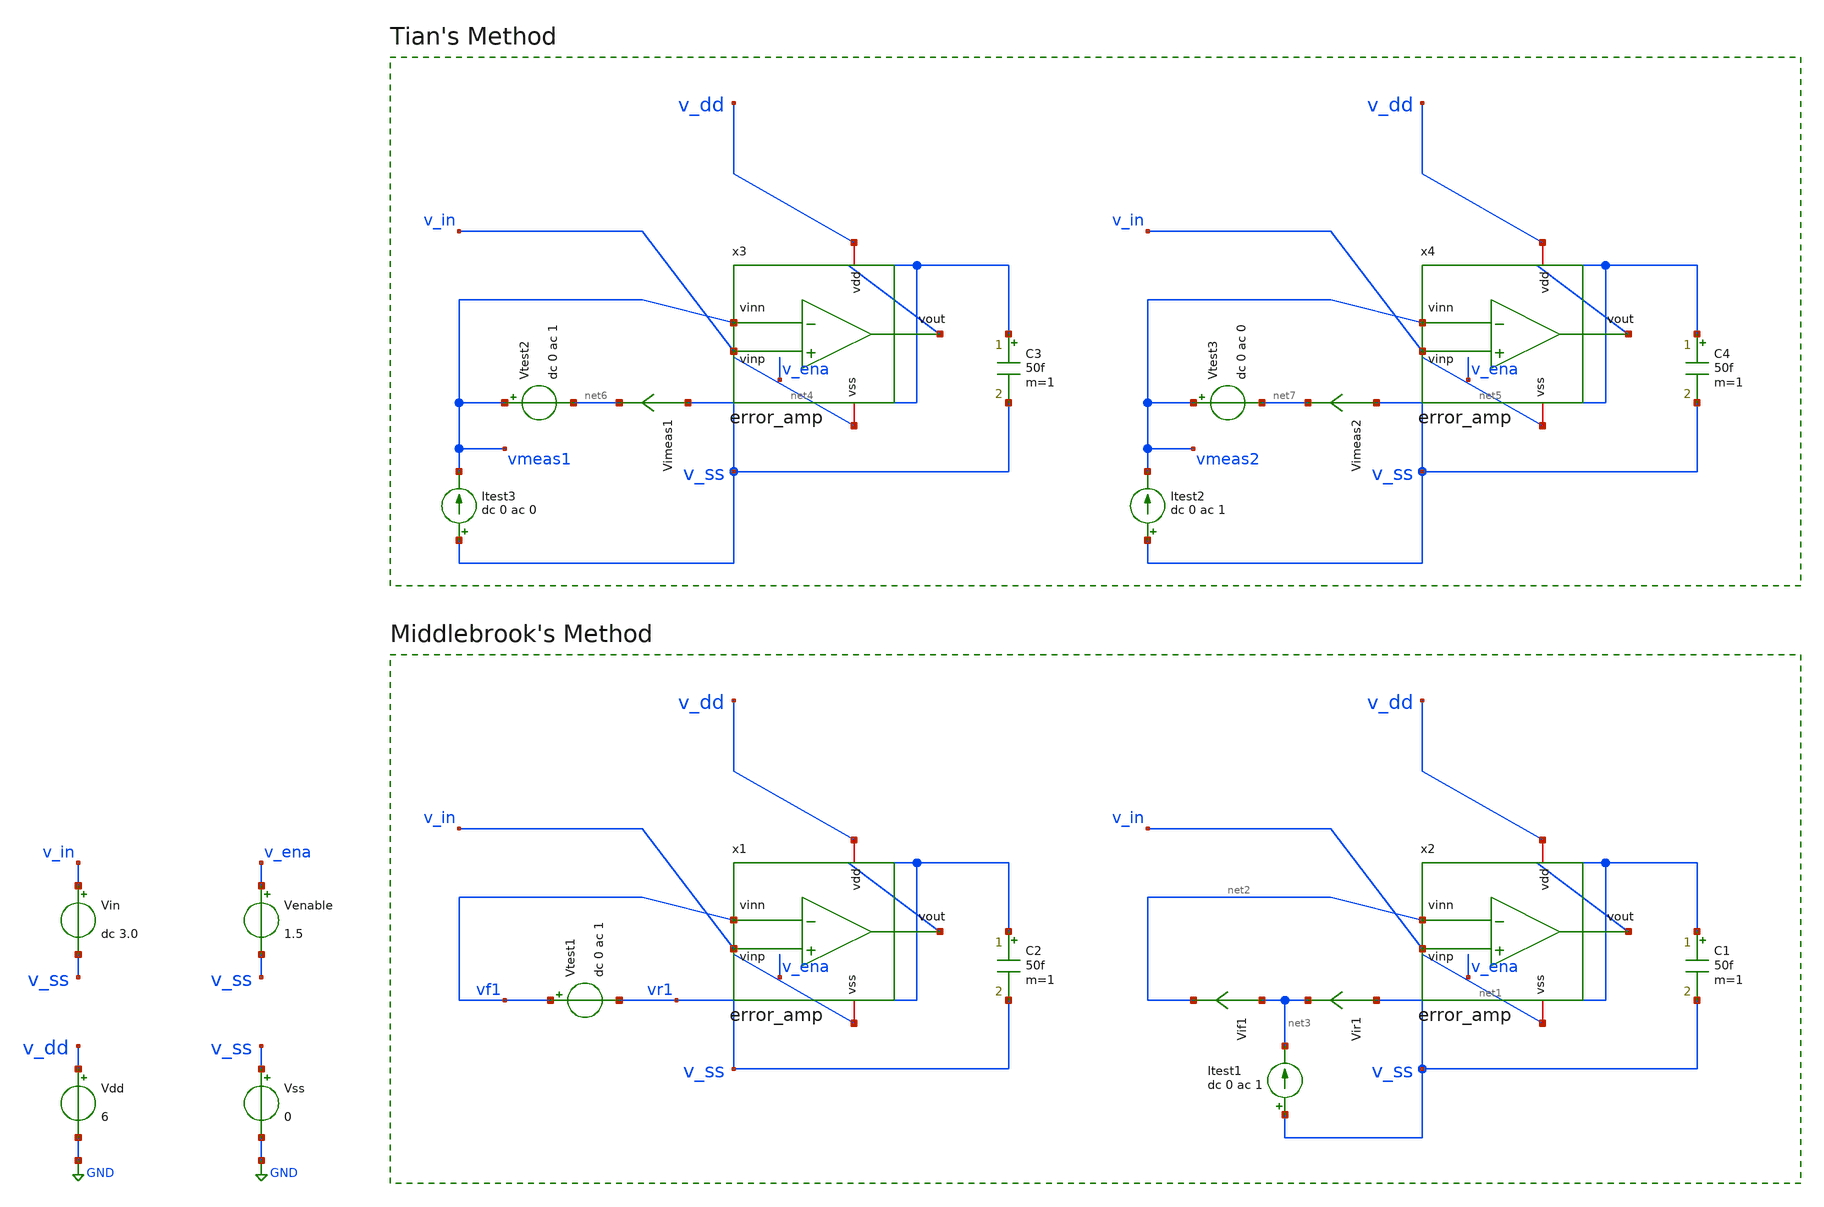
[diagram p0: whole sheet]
** sch_path: analog-db/drawings/ldo-005-ti-ldo-buffer-ref/gf180/error_amp/error_amp_tb-loopgain.sch
* (c) 2024 H. Pretl, S. Dorrer, Apache-2.0 license
**.subckt error_amp_tb-loopgain
Vdd v_dd GND 6
Vss v_ss GND 0
Vin v_in v_ss dc 3.0
Venable v_ena v_ss 1.5
C2 vr1 v_ss 50f m=1
x1 v_dd vr1 v_in vf1 v_ss error_amp
Vtest1 vf1 vr1 dc 0 ac 1
C1 net1 v_ss 50f m=1
x2 v_dd net1 v_in net2 v_ss error_amp
Vir1 net1 net3 0
Vif1 net3 net2 0
Itest1 v_ss net3 dc 0 ac 1
C3 net4 v_ss 50f m=1
x3 v_dd net4 v_in vmeas1 v_ss error_amp
C4 net5 v_ss 50f m=1
x4 v_dd net5 v_in vmeas2 v_ss error_amp
Itest3 v_ss vmeas1 dc 0 ac 0
Vtest2 vmeas1 net6 dc 0 ac 1
Vimeas1 net4 net6 0
Itest2 v_ss vmeas2 dc 0 ac 1
Vtest3 vmeas2 net7 dc 0 ac 0
Vimeas2 net5 net7 0
**** begin user architecture code
 .include $::180MCU_MODELS/design.ngspice
.lib $::180MCU_MODELS/sm141064.ngspice typical
.lib $::180MCU_MODELS/sm141064.ngspice res_typical



.param temp=27
.options savecurrents reltol=1e-3 abstol=1e-12 gmin=1e-15
.control
save all

* Operating Point Analysis
op
remzerovec
write ota-5t_tb-loopgain.raw
set appendwrite

* AC Analysis
ac dec 101 1 100G
remzerovec
write ota-5t_tb-loopgain.raw
set appendwrite

* Middlebrook's Method
let tv=-v(vr1)/v(vf1)
let ti=-i(vir1)/i(vif1)
let tmb=(tv*ti - 1)/(tv + ti + 2)

plot db(tmb) ylabel 'Magnitude - Middlebrook'
plot 180/pi*cphase(tmb) ylabel 'Phase - Middlebrook'

* Tian's Method
* vtest=0, itest=1:
let A=i(Vimeas2)
let C=v(vmeas2)

* vtest=1, itest=0:
let B=i(Vimeas1)
let D=v(vmeas1)
let ttian=(A*D-B*C-A)/(2*(B*C-A*D)+A-D+1)

plot db(ttian) ylabel 'Magnitude - Tian'
plot 180/pi*cphase(ttian) ylabel 'Phase - Tian'

* Middlebrook vs. Tian
plot db(tmb) db(ttian) ylabel 'Magnitude'
plot 180/pi*cphase(tmb) 180/pi*cphase(ttian) ylabel 'Phase'

write ota-5t_tb-loopgain.raw

*quit
.endc


**** end user architecture code
**.ends

* expanding   symbol:  ldo-005-ti-ldo-buffer-ref/gf180/error_amp/error_amp.sym # of pins=5
** sym_path: analog-db/circuits/amp_032_ti_ldo_error_selfbias/pdk/gf180mcu/schematic/error_amp.sym
** sch_path: analog-db/circuits/amp_032_ti_ldo_error_selfbias/pdk/gf180mcu/schematic/error_amp.sch
.subckt error_amp vdd vout vinp vinn vss
*.iopin vdd
*.iopin vss
*.ipin vinp
*.opin vout
*.ipin vinn
XM2 net_b vinp net_c vss nfet_06v0 L=0.7u W=68.542u nf=1 ad='int((nf+1)/2) * W/nf * 0.18u' as='int((nf+2)/2) * W/nf * 0.18u'
+ pd='2*int((nf+1)/2) * (W/nf + 0.18u)' ps='2*int((nf+2)/2) * (W/nf + 0.18u)' nrd='0.18u / W' nrs='0.18u / W'
+ sa=0 sb=0 sd=0 m=1
XM3m net_a net_d vdd vdd pfet_06v0 L=0.5u W=69.545u nf=1 ad='int((nf+1)/2) * W/nf * 0.18u' as='int((nf+2)/2) * W/nf * 0.18u'
+ pd='2*int((nf+1)/2) * (W/nf + 0.18u)' ps='2*int((nf+2)/2) * (W/nf + 0.18u)' nrd='0.18u / W' nrs='0.18u / W'
+ sa=0 sb=0 sd=0 m=1
XM4 net_f net_a net_d vdd pfet_06v0 L=0.5u W=10u nf=1 ad='int((nf+1)/2) * W/nf * 0.18u' as='int((nf+2)/2) * W/nf * 0.18u'
+ pd='2*int((nf+1)/2) * (W/nf + 0.18u)' ps='2*int((nf+2)/2) * (W/nf + 0.18u)' nrd='0.18u / W' nrs='0.18u / W'
+ sa=0 sb=0 sd=0 m=1
XM5 net_b net_d vdd vdd pfet_06v0 L=0.5u W=69.545u nf=1 ad='int((nf+1)/2) * W/nf * 0.18u' as='int((nf+2)/2) * W/nf * 0.18u'
+ pd='2*int((nf+1)/2) * (W/nf + 0.18u)' ps='2*int((nf+2)/2) * (W/nf + 0.18u)' nrd='0.18u / W' nrs='0.18u / W'
+ sa=0 sb=0 sd=0 m=1
XM6 vout net_b vdd vdd pfet_06v0 L=3.8349u W=20u nf=1 ad='int((nf+1)/2) * W/nf * 0.18u' as='int((nf+2)/2) * W/nf * 0.18u'
+ pd='2*int((nf+1)/2) * (W/nf + 0.18u)' ps='2*int((nf+2)/2) * (W/nf + 0.18u)' nrd='0.18u / W' nrs='0.18u / W'
+ sa=0 sb=0 sd=0 m=1
Cc net1 vout 6.7168p m=1
XRZ net_b net1 vdd ppolyf_u_3k r_width=1u r_length=9.476u m=1
XM1 net_a vinn net_c vss nfet_06v0 L=0.7u W=68.542u nf=1 ad='int((nf+1)/2) * W/nf * 0.18u' as='int((nf+2)/2) * W/nf * 0.18u'
+ pd='2*int((nf+1)/2) * (W/nf + 0.18u)' ps='2*int((nf+2)/2) * (W/nf + 0.18u)' nrd='0.18u / W' nrs='0.18u / W'
+ sa=0 sb=0 sd=0 m=1
XM_mirror_error_amp_ref net2 net2 vss vss nfet_06v0 L=2u W=34.533u nf=1 ad='int((nf+1)/2) * W/nf * 0.18u'
+ as='int((nf+2)/2) * W/nf * 0.18u' pd='2*int((nf+1)/2) * (W/nf + 0.18u)' ps='2*int((nf+2)/2) * (W/nf + 0.18u)'
+ nrd='0.18u / W' nrs='0.18u / W' sa=0 sb=0 sd=0 m=1
XM_mirror_f net_f net2 vss vss nfet_06v0 L=2u W=5u nf=1 ad='int((nf+1)/2) * W/nf * 0.18u' as='int((nf+2)/2) * W/nf * 0.18u'
+ pd='2*int((nf+1)/2) * (W/nf + 0.18u)' ps='2*int((nf+2)/2) * (W/nf + 0.18u)' nrd='0.18u / W' nrs='0.18u / W'
+ sa=0 sb=0 sd=0 m=1
XM_mirror_c net_c net2 vss vss nfet_06v0 L=2u W=34.533u nf=1 ad='int((nf+1)/2) * W/nf * 0.18u' as='int((nf+2)/2) * W/nf * 0.18u'
+ pd='2*int((nf+1)/2) * (W/nf + 0.18u)' ps='2*int((nf+2)/2) * (W/nf + 0.18u)' nrd='0.18u / W' nrs='0.18u / W'
+ sa=0 sb=0 sd=0 m=1
XM_mirror_ea_out vout net2 vss vss nfet_06v0 L=2u W=34.533u nf=1 ad='int((nf+1)/2) * W/nf * 0.18u' as='int((nf+2)/2) * W/nf * 0.18u'
+ pd='2*int((nf+1)/2) * (W/nf + 0.18u)' ps='2*int((nf+2)/2) * (W/nf + 0.18u)' nrd='0.18u / W' nrs='0.18u / W'
+ sa=0 sb=0 sd=0 m=1
XM_bias net2 net2 vdd vdd pfet_06v0 L=2u W=6.3111u nf=1 ad='int((nf+1)/2) * W/nf * 0.18u' as='int((nf+2)/2) * W/nf * 0.18u'
+ pd='2*int((nf+1)/2) * (W/nf + 0.18u)' ps='2*int((nf+2)/2) * (W/nf + 0.18u)' nrd='0.18u / W' nrs='0.18u / W'
+ sa=0 sb=0 sd=0 m=1
.ends

.GLOBAL GND
.end
